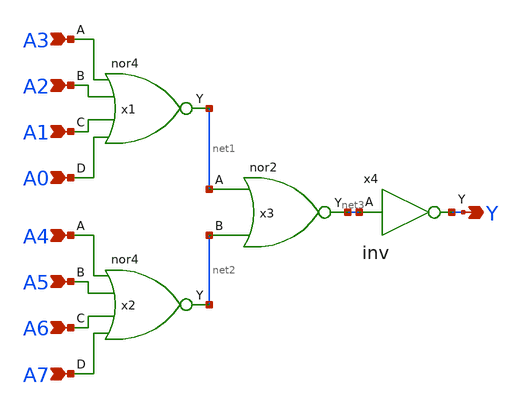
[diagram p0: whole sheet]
** sch_path: design/xschem/NOR/nor8.sch
**.subckt nor8 Y A4 A5 A6 A7 A0 A3 A2 A1
*.opin Y
*.ipin A4
*.ipin A5
*.ipin A6
*.ipin A7
*.ipin A0
*.ipin A3
*.ipin A2
*.ipin A1
x1 A3 A2 A1 A0 VSS VDD net1 nor4
x2 A4 A5 A6 A7 VSS VDD net2 nor4
x3 net1 net2 VSS VDD net3 nor2
x4 net3 VSS VDD Y inv
**.ends
.end
